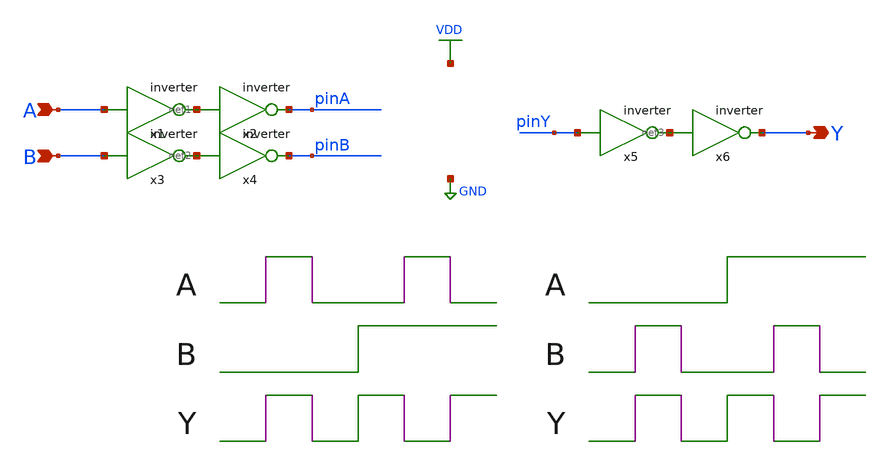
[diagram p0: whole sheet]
** sch_path: xor_delay.sch
**.subckt xor_delay A B Y
*.ipin A
*.ipin B
*.opin Y
x1 net1 A inverter
x2 pinA net1 inverter
x3 net2 B inverter
x6 Y net3 inverter
x4 pinB net2 inverter
x5 net3 pinY inverter
**** begin user architecture code



VP VDD 0 dc 1.8

// XOR_A TEST

VA A 0 dc 0
VB B 0 dc 0

.control
save a b c d y pinA pinB pinY
alter @va[PULSE] [ 0 1.8 1n 40p 40p 1n 3n ]
alter @vb[PULSE] [ 0 1.8 3n 40p 40p 4n 8n ]
tran 10p 6n
meas tran  in1 FIND time WHEN v(pina)=0.9 RISE=1 > NUL
meas tran out1 FIND time WHEN v(piny)=0.9 RISE=1 > NUL
meas tran  in2 FIND time WHEN v(pina)=0.9 FALL=1 > NUL
meas tran out2 FIND time WHEN v(piny)=0.9 FALL=1 > NUL
meas tran  in3 FIND time WHEN v(pina)=0.9 RISE=2 > NUL
meas tran out3 FIND time WHEN v(piny)=0.9 FALL=2 > NUL
meas tran  in4 FIND time WHEN v(pina)=0.9 FALL=2 > NUL
meas tran out4 FIND time WHEN v(piny)=0.9 RISE=3 > NUL

let calc1 = out1 - in1
set delayxa1 = $&calc1
let calc2 = out2 - in2
set delayxa2 = $&calc2
let calc3 = out3 - in3
set delayxa3 = $&calc3
let calc4 = out4 - in4
set delayxa4 = $&calc4

alter @vb[PULSE] [ 0 1.8 1n 40p 40p 1n 3n ]
alter @va[PULSE] [ 0 1.8 3n 40p 40p 4n 8n ]
tran 10p 6n
meas tran  in5 FIND time WHEN v(pinb)=0.9 RISE=1 > NUL
meas tran out5 FIND time WHEN v(piny)=0.9 RISE=1 > NUL
meas tran  in6 FIND time WHEN v(pinb)=0.9 FALL=1 > NUL
meas tran out6 FIND time WHEN v(piny)=0.9 FALL=1 > NUL
meas tran  in7 FIND time WHEN v(pinb)=0.9 RISE=2 > NUL
meas tran out7 FIND time WHEN v(piny)=0.9 FALL=2 > NUL
meas tran  in8 FIND time WHEN v(pinb)=0.9 FALL=2 > NUL
meas tran out8 FIND time WHEN v(piny)=0.9 RISE=3 > NUL

let calc5 = out5 - in5
set delayxa5 = $&calc5
let calc6 = out6 - in6
set delayxa6 = $&calc6
let calc7 = out7 - in7
set delayxa7 = $&calc7
let calc8 = out8 - in8
set delayxa8 = $&calc8


echo '*** XOR1 DELAY CASE 1 ***'
echo 'A(LH) when B(L) ='{$delayxa1}
echo 'A(HL) when B(L) ='{$delayxa2}
echo 'A(LH) when B(H) ='{$delayxa3}
echo 'A(HL) when B(H) ='{$delayxa4}

echo '*** XOR1 DELAY CASE 2 ***'
echo 'B(LH) when A(L) ='{$delayxa5}
echo 'B(HL) when A(L) ='{$delayxa6}
echo 'B(LH) when A(H) ='{$delayxa7}
echo 'B(HL) when A(H) ='{$delayxa8}
.endc



 .param mc_mm_switch=0
.param mc_pr_switch=0
.include $::SKYWATER_MODELS/corners/tt.spice
.include $::SKYWATER_MODELS/r+c/res_typical__cap_typical.spice
.include $::SKYWATER_MODELS/r+c/res_typical__cap_typical__lin.spice
.include $::SKYWATER_MODELS/corners/tt/specialized_cells.spice
.include $::SKYWATER_STDCELLS/sky130_fd_sc_hd.spice

**** end user architecture code
**.ends

* expanding   symbol:  inverter.sym # of pins=2
** sym_path: inverter.sym
** sch_path: inverter.sch
.subckt inverter Y A
*.ipin A
*.opin Y
XM1 Y A VDD VDD sky130_fd_pr__pfet_01v8 L=0.15 W=2.2 nf=1 ad='int((nf+1)/2) * W/nf * 0.29' as='int((nf+2)/2) * W/nf * 0.29'
+ pd='2*int((nf+1)/2) * (W/nf + 0.29)' ps='2*int((nf+2)/2) * (W/nf + 0.29)' nrd='0.29 / W' nrs='0.29 / W'
+ sa=0 sb=0 sd=0 mult=1 m=1
XM2 Y A GND GND sky130_fd_pr__nfet_01v8 L=0.15 W=1 nf=1 ad='int((nf+1)/2) * W/nf * 0.29' as='int((nf+2)/2) * W/nf * 0.29'
+ pd='2*int((nf+1)/2) * (W/nf + 0.29)' ps='2*int((nf+2)/2) * (W/nf + 0.29)' nrd='0.29 / W' nrs='0.29 / W'
+ sa=0 sb=0 sd=0 mult=1 m=1
.ends

.GLOBAL VDD
.GLOBAL GND
.end
